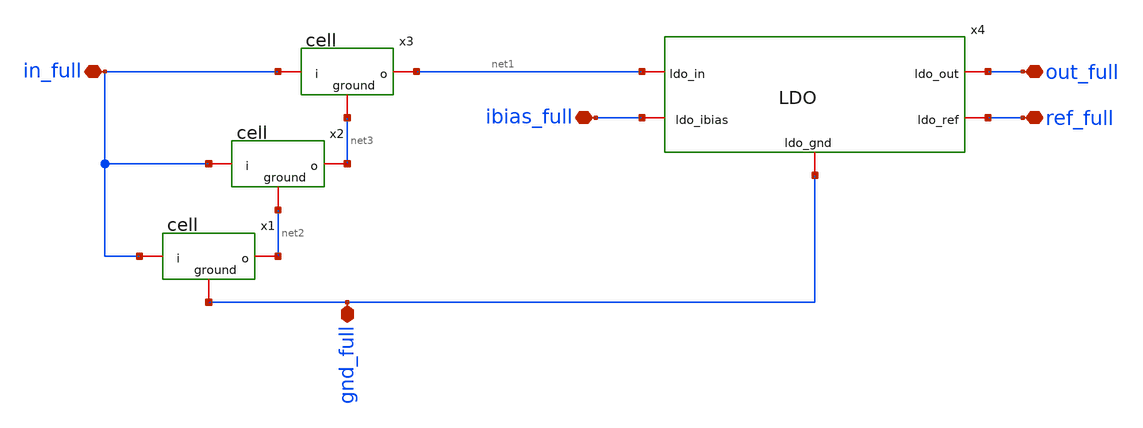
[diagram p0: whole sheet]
** sch_path: xschem/ret_ldo.sch
**.subckt ret_ldo in_full gnd_full ibias_full ref_full out_full
*.iopin in_full
*.iopin gnd_full
*.iopin ibias_full
*.iopin ref_full
*.iopin out_full
x1 net2 in_full gnd_full cell
x2 net3 in_full net2 cell
x4 net1 out_full ibias_full ref_full gnd_full LDO
x3 net1 in_full net3 cell
**.ends

* expanding   symbol:  cell.sym # of pins=3
** sym_path: xschem/cell.sym
** sch_path: xschem/cell.sch
.subckt cell o i ground
*.iopin ground
*.iopin o
*.iopin i
XM10 net1 net1 ground net1 sky130_fd_pr__pfet_01v8_lvt L=0.35 W=40 nf=5 ad='int((5 + 1)/2) * 40 / 5 * 0.29'
+ as='int((5 + 2)/2) * 40 / 5 * 0.29' pd='2*int((5 + 1)/2) * (40 / 5 + 0.29)' ps='2*int((5 + 2)/2) * (40 / 5 + 0.29)'
+ nrd='0.29 / 40 ' nrs='0.29 / 40 ' sa=0 sb=0 sd=0 mult=1 m=1
XM1 o o net1 o sky130_fd_pr__pfet_01v8_lvt L=0.35 W=40 nf=5 ad='int((5 + 1)/2) * 40 / 5 * 0.29' as='int((5 + 2)/2) * 40 / 5 * 0.29'
+ pd='2*int((5 + 1)/2) * (40 / 5 + 0.29)' ps='2*int((5 + 2)/2) * (40 / 5 + 0.29)' nrd='0.29 / 40 ' nrs='0.29 / 40 '
+ sa=0 sb=0 sd=0 mult=1 m=1
XC3 o ground sky130_fd_pr__cap_mim_m3_1 W=30 L=30 MF=3 m=3
XC2 net1 i sky130_fd_pr__cap_mim_m3_1 W=30 L=30 MF=1 m=1
.ends


* expanding   symbol:  LDO.sym # of pins=5
** sym_path: xschem/LDO.sym
** sch_path: xschem/LDO.sch
.subckt LDO ldo_in ldo_out ldo_ibias ldo_ref ldo_gnd
*.iopin ldo_out
*.iopin ldo_in
*.iopin ldo_gnd
*.iopin ldo_ref
*.iopin ldo_ibias
x1 ldo_in ldo_out ldo_ref net1 ldo_ibias ldo_gnd Ota_esq
XM1 ldo_in net1 ldo_out ldo_gnd sky130_fd_pr__nfet_03v3_nvt L=0.5 W=10 nf=1 ad='int((nf+1)/2) * W/nf * 0.29'
+ as='int((nf+2)/2) * W/nf * 0.29' pd='2*int((nf+1)/2) * (W/nf + 0.29)' ps='2*int((nf+2)/2) * (W/nf + 0.29)'
+ nrd='0.29 / W' nrs='0.29 / W' sa=0 sb=0 sd=0 mult=1 m=1
.ends


* expanding   symbol:  Ota_esq.sym # of pins=6
** sym_path: xschem/Ota_esq.sym
** sch_path: xschem/Ota_esq.sch
.subckt Ota_esq VDD Vin Vip Vout Ibias VSS
*.ipin Vin
*.ipin Vip
*.iopin VDD
*.iopin VSS
*.iopin Ibias
*.opin Vout
XC1 net2 Vout sky130_fd_pr__cap_mim_m3_1 W=23 L=23 MF=1 m=1
XM3 VSS net1 net1 VSS sky130_fd_pr__nfet_g5v0d10v5 L=0.5 W=7 nf=1 ad='int((nf+1)/2) * W/nf * 0.29' as='int((nf+2)/2) * W/nf * 0.29'
+ pd='2*int((nf+1)/2) * (W/nf + 0.29)' ps='2*int((nf+2)/2) * (W/nf + 0.29)' nrd='0.29 / W' nrs='0.29 / W'
+ sa=0 sb=0 sd=0 mult=1 m=1
XM1 net1 Vin net3 net3 sky130_fd_pr__pfet_g5v0d10v5 L=0.5 W=2 nf=1 ad='int((nf+1)/2) * W/nf * 0.29' as='int((nf+2)/2) * W/nf * 0.29'
+ pd='2*int((nf+1)/2) * (W/nf + 0.29)' ps='2*int((nf+2)/2) * (W/nf + 0.29)' nrd='0.29 / W' nrs='0.29 / W'
+ sa=0 sb=0 sd=0 mult=1 m=1
XM2 net3 Vip net2 net3 sky130_fd_pr__pfet_g5v0d10v5 L=0.5 W=2 nf=1 ad='int((nf+1)/2) * W/nf * 0.29' as='int((nf+2)/2) * W/nf * 0.29'
+ pd='2*int((nf+1)/2) * (W/nf + 0.29)' ps='2*int((nf+2)/2) * (W/nf + 0.29)' nrd='0.29 / W' nrs='0.29 / W'
+ sa=0 sb=0 sd=0 mult=1 m=1
XM4 net2 net1 VSS VSS sky130_fd_pr__nfet_g5v0d10v5 L=0.5 W=7 nf=1 ad='int((nf+1)/2) * W/nf * 0.29' as='int((nf+2)/2) * W/nf * 0.29'
+ pd='2*int((nf+1)/2) * (W/nf + 0.29)' ps='2*int((nf+2)/2) * (W/nf + 0.29)' nrd='0.29 / W' nrs='0.29 / W'
+ sa=0 sb=0 sd=0 mult=1 m=1
XM7 Vout net2 VSS VSS sky130_fd_pr__nfet_g5v0d10v5 L=1 W=21 nf=7 ad='int((nf+1)/2) * W/nf * 0.29' as='int((nf+2)/2) * W/nf * 0.29'
+ pd='2*int((nf+1)/2) * (W/nf + 0.29)' ps='2*int((nf+2)/2) * (W/nf + 0.29)' nrd='0.29 / W' nrs='0.29 / W'
+ sa=0 sb=0 sd=0 mult=1 m=1
XM8 VDD Ibias Ibias VDD sky130_fd_pr__pfet_g5v0d10v5 L=1 W=24 nf=8 ad='int((nf+1)/2) * W/nf * 0.29' as='int((nf+2)/2) * W/nf * 0.29'
+ pd='2*int((nf+1)/2) * (W/nf + 0.29)' ps='2*int((nf+2)/2) * (W/nf + 0.29)' nrd='0.29 / W' nrs='0.29 / W'
+ sa=0 sb=0 sd=0 mult=1 m=1
XM5 net3 Ibias VDD VDD sky130_fd_pr__pfet_g5v0d10v5 L=1 W=24 nf=8 ad='int((nf+1)/2) * W/nf * 0.29' as='int((nf+2)/2) * W/nf * 0.29'
+ pd='2*int((nf+1)/2) * (W/nf + 0.29)' ps='2*int((nf+2)/2) * (W/nf + 0.29)' nrd='0.29 / W' nrs='0.29 / W'
+ sa=0 sb=0 sd=0 mult=1 m=1
XM6 Vout Ibias VDD VDD sky130_fd_pr__pfet_g5v0d10v5 L=1 W=39 nf=13 ad='int((nf+1)/2) * W/nf * 0.29' as='int((nf+2)/2) * W/nf * 0.29'
+ pd='2*int((nf+1)/2) * (W/nf + 0.29)' ps='2*int((nf+2)/2) * (W/nf + 0.29)' nrd='0.29 / W' nrs='0.29 / W'
+ sa=0 sb=0 sd=0 mult=1 m=1
.ends

.end
